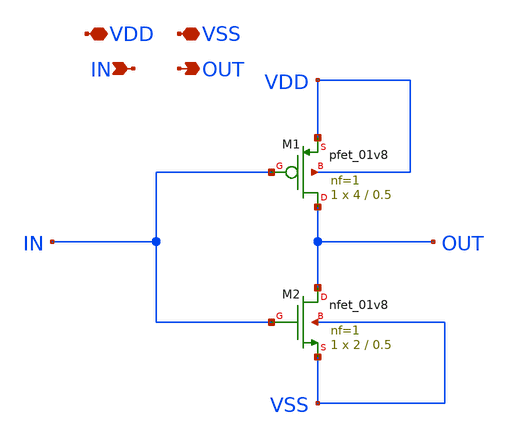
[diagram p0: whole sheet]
** sch_path: Xschem/PLL_TOP_Schematics/INV_Mux.sch
**.subckt INV_Mux VDD VSS IN OUT
*.iopin VDD
*.iopin VSS
*.ipin IN
*.opin OUT
XM1 OUT IN VDD VDD sky130_fd_pr__pfet_01v8 L=0.5 W=4 nf=1 ad='int((nf+1)/2) * W/nf * 0.29' as='int((nf+2)/2) * W/nf * 0.29'
+ pd='2*int((nf+1)/2) * (W/nf + 0.29)' ps='2*int((nf+2)/2) * (W/nf + 0.29)' nrd='0.29 / W' nrs='0.29 / W'
+ sa=0 sb=0 sd=0 mult=1 m=1
XM2 OUT IN VSS VSS sky130_fd_pr__nfet_01v8 L=0.5 W=2 nf=1 ad='int((nf+1)/2) * W/nf * 0.29' as='int((nf+2)/2) * W/nf * 0.29'
+ pd='2*int((nf+1)/2) * (W/nf + 0.29)' ps='2*int((nf+2)/2) * (W/nf + 0.29)' nrd='0.29 / W' nrs='0.29 / W'
+ sa=0 sb=0 sd=0 mult=1 m=1
**.ends
.end
